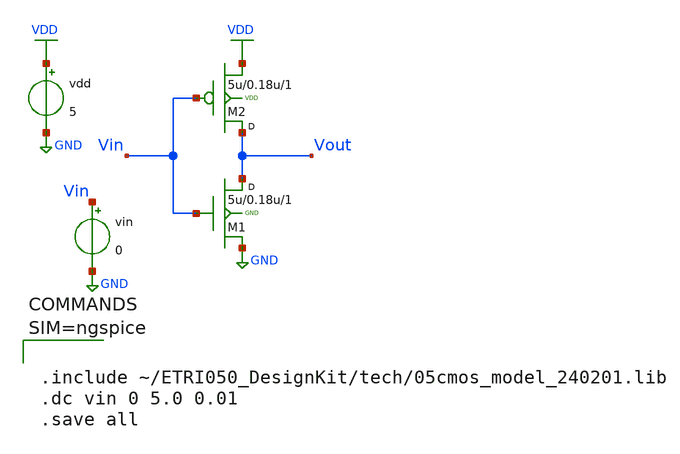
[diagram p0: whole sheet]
** sch_path: Tutorials/1-1_Inverter_XSchem/inverter1/inverter1.sch
**.subckt inverter1
M1 Vout Vin GND GND nfet w=5u l=0.18u m=1
M2 Vout Vin VDD VDD pfet w=5u l=0.18u m=1
vdd VDD GND 5
vin Vin GND 0
**** begin user architecture code



.include ~/ETRI050_DesignKit/tech/05cmos_model_240201.lib
.dc vin 0 5.0 0.01
.save all



**** end user architecture code
**.ends
.GLOBAL VDD
.GLOBAL GND
.end
